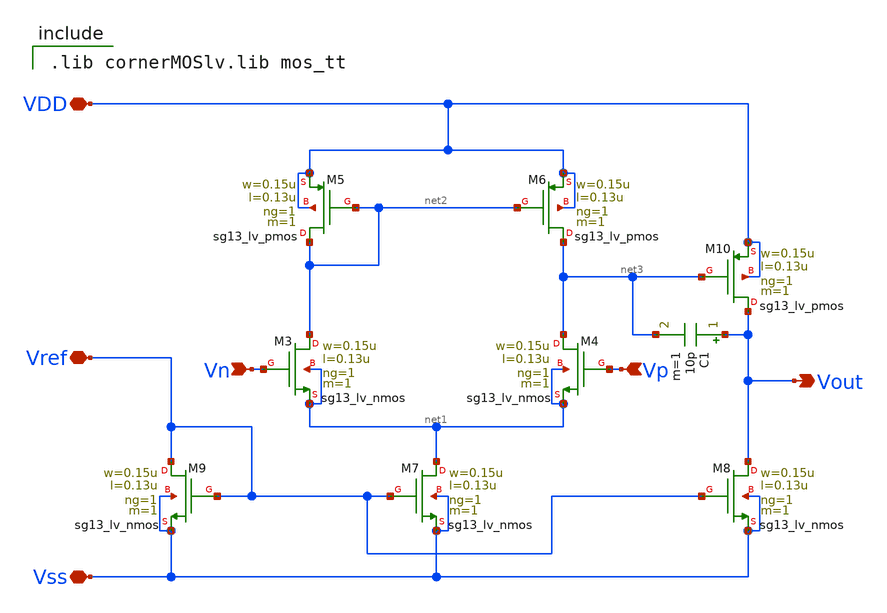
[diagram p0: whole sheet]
** sch_path: designs/opamp/opamp.sch
**.subckt opamp Vn Vp Vout VDD Vref Vss
*.ipin Vn
*.ipin Vp
*.opin Vout
*.iopin VDD
*.iopin Vref
*.iopin Vss
XM3 net2 Vn net1 net1 sg13_lv_nmos w=0.15u l=0.13u ng=1 m=1 mm_ok=1
XM4 net3 Vp net1 net1 sg13_lv_nmos w=0.15u l=0.13u ng=1 m=1 mm_ok=1
XM5 net2 net2 VDD VDD sg13_lv_pmos w=0.15u l=0.13u ng=1 m=1 mm_ok=1
XM6 net3 net2 VDD VDD sg13_lv_pmos w=0.15u l=0.13u ng=1 m=1 mm_ok=1
XM7 net1 Vref Vss Vss sg13_lv_nmos w=0.15u l=0.13u ng=1 m=1 mm_ok=1
XM8 Vout Vref Vss Vss sg13_lv_nmos w=0.15u l=0.13u ng=1 m=1 mm_ok=1
XM9 Vref Vref Vss Vss sg13_lv_nmos w=0.15u l=0.13u ng=1 m=1 mm_ok=1
XM10 Vout net3 VDD VDD sg13_lv_pmos w=0.15u l=0.13u ng=1 m=1 mm_ok=1
C1 Vout net3 10p m=1
**** begin user architecture code

.lib cornerMOSlv.lib mos_tt

**** end user architecture code
**.ends
.end
